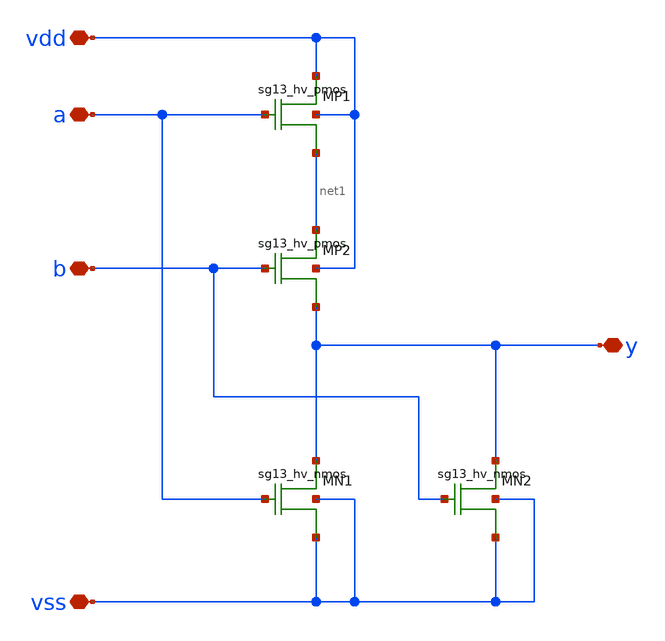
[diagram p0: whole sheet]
** sch_path: xschem/logic_gates/NORHV.sch
**.subckt NORHV vdd vss y a b
*.iopin vdd
*.iopin vss
*.iopin y
*.iopin a
*.iopin b
XMP1 vdd a net1 vdd sg13_hv_pmos w=4.0u l=0.45u ng=1 m=1
XMP2 net1 b y vdd sg13_hv_pmos w=4.0u l=0.45u ng=1 m=1
XMN1 y a vss vss sg13_hv_nmos w=1.0u l=0.45u ng=1 m=1
XMN2 y b vss vss sg13_hv_nmos w=1.0u l=0.45u ng=1 m=1
**.ends
.end
